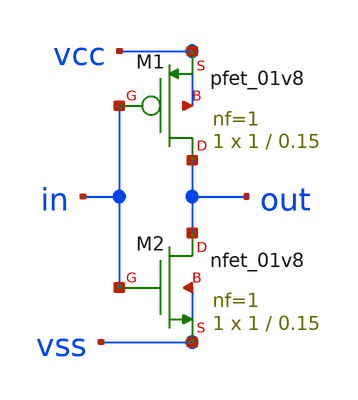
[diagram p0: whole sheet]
** sch_path: first.sch
**.subckt first
XM1 out in vcc vcc sky130_fd_pr__pfet_01v8 L=0.15 W=1 nf=1 ad='int((nf+1)/2) * W/nf * 0.29' as='int((nf+2)/2) * W/nf * 0.29'
+ pd='2*int((nf+1)/2) * (W/nf + 0.29)' ps='2*int((nf+2)/2) * (W/nf + 0.29)' nrd='0.29 / W' nrs='0.29 / W'
+ sa=0 sb=0 sd=0 mult=1 m=1
XM2 out in vss vss sky130_fd_pr__nfet_01v8 L=0.15 W=1 nf=1 ad='int((nf+1)/2) * W/nf * 0.29' as='int((nf+2)/2) * W/nf * 0.29'
+ pd='2*int((nf+1)/2) * (W/nf + 0.29)' ps='2*int((nf+2)/2) * (W/nf + 0.29)' nrd='0.29 / W' nrs='0.29 / W'
+ sa=0 sb=0 sd=0 mult=1 m=1
**.ends
.end
